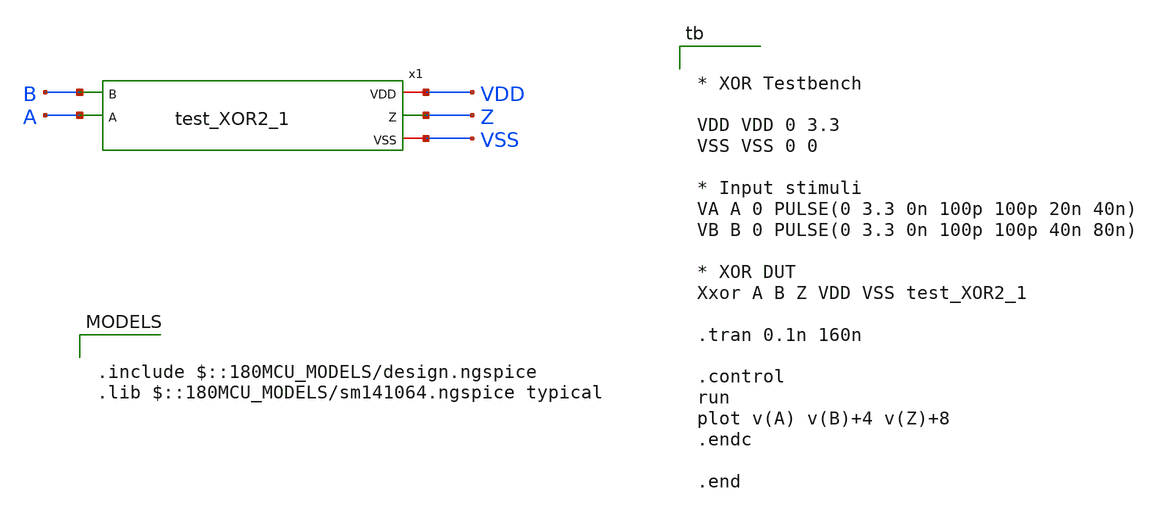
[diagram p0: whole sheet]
** sch_path: xschem/tb_fail_XOR2_1.sch
**.subckt tb_fail_XOR2_1
x1 VDD Z B A VSS test_XOR2_1
**** begin user architecture code


* XOR Testbench

VDD VDD 0 3.3
VSS VSS 0 0

* Input stimuli
VA A 0 PULSE(0 3.3 0n 100p 100p 20n 40n)
VB B 0 PULSE(0 3.3 0n 100p 100p 40n 80n)

* XOR DUT
Xxor A B Z VDD VSS test_XOR2_1

.tran 0.1n 160n

.control
run
plot v(A) v(B)+4 v(Z)+8
.endc

.end


.include $::180MCU_MODELS/design.ngspice
.lib $::180MCU_MODELS/sm141064.ngspice typical

**** end user architecture code
**.ends
.end
